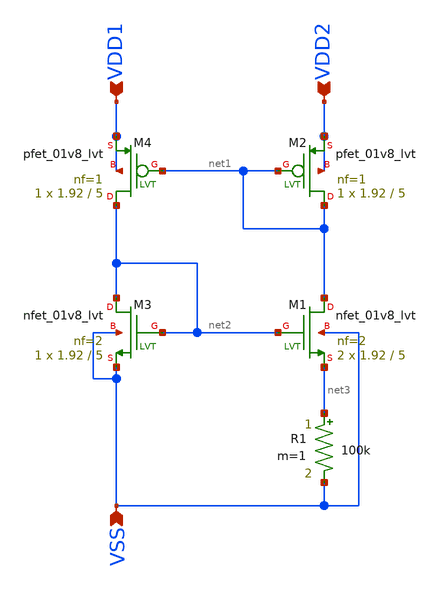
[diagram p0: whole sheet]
** sch_path: design/LELO_SVOD_SKY130A/LELO_PTAT_CURRENT.sch
**.subckt LELO_PTAT_CURRENT VDD1 VSS VDD2
*.ipin VDD1
*.ipin VSS
*.ipin VDD2
R1 net3 VSS 100k m=1
XM1 net1 net2 net3 VSS sky130_fd_pr__nfet_01v8_lvt L=5 W=1.92 nf=2 ad='int((2 + 1)/2) * 1.92 / 2 * 0.29'
+ as='int((2 + 2)/2) * 1.92 / 2 * 0.29' pd='2*int((2 + 1)/2) * (1.92 / 2 + 0.29)' ps='2*int((2 + 2)/2) * (1.92 / 2 + 0.29)'
+ nrd='0.29 / 1.92 ' nrs='0.29 / 1.92 ' sa=0 sb=0 sd=0 mult=2 m=2
XM2 net1 net1 VDD2 VDD2 sky130_fd_pr__pfet_01v8_lvt L=5 W=1.92 nf=1 ad='int((1 + 1)/2) * 1.92 / 1 * 0.29'
+ as='int((1 + 2)/2) * 1.92 / 1 * 0.29' pd='2*int((1 + 1)/2) * (1.92 / 1 + 0.29)' ps='2*int((1 + 2)/2) * (1.92 / 1 + 0.29)'
+ nrd='0.29 / 1.92 ' nrs='0.29 / 1.92 ' sa=0 sb=0 sd=0 mult=1 m=1
XM3 net2 net2 VSS VSS sky130_fd_pr__nfet_01v8_lvt L=5 W=1.92 nf=2 ad='int((2 + 1)/2) * 1.92 / 2 * 0.29'
+ as='int((2 + 2)/2) * 1.92 / 2 * 0.29' pd='2*int((2 + 1)/2) * (1.92 / 2 + 0.29)' ps='2*int((2 + 2)/2) * (1.92 / 2 + 0.29)'
+ nrd='0.29 / 1.92 ' nrs='0.29 / 1.92 ' sa=0 sb=0 sd=0 mult=1 m=1
XM4 net2 net1 VDD1 VDD1 sky130_fd_pr__pfet_01v8_lvt L=5 W=1.92 nf=1 ad='int((1 + 1)/2) * 1.92 / 1 * 0.29'
+ as='int((1 + 2)/2) * 1.92 / 1 * 0.29' pd='2*int((1 + 1)/2) * (1.92 / 1 + 0.29)' ps='2*int((1 + 2)/2) * (1.92 / 1 + 0.29)'
+ nrd='0.29 / 1.92 ' nrs='0.29 / 1.92 ' sa=0 sb=0 sd=0 mult=1 m=1
**.ends
.end
